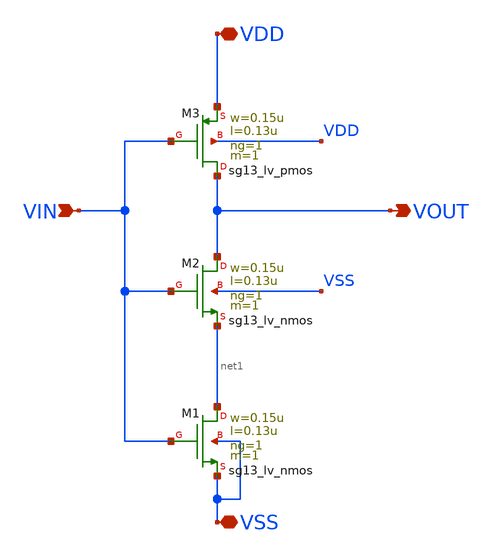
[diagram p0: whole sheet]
** sch_path: ADC8711-main/schematic/xschem/INV05.sch
**.subckt INV05 VDD VSS VOUT VIN
*.iopin VDD
*.iopin VSS
*.opin VOUT
*.ipin VIN
XM1 net1 VIN VSS VSS sg13_lv_nmos w=0.15u l=0.13u ng=1 m=1 mm_ok=1
XM3 VOUT VIN VDD VDD sg13_lv_pmos w=0.15u l=0.13u ng=1 m=1 mm_ok=1
XM2 VOUT VIN net1 VSS sg13_lv_nmos w=0.15u l=0.13u ng=1 m=1 mm_ok=1
**.ends
.end
